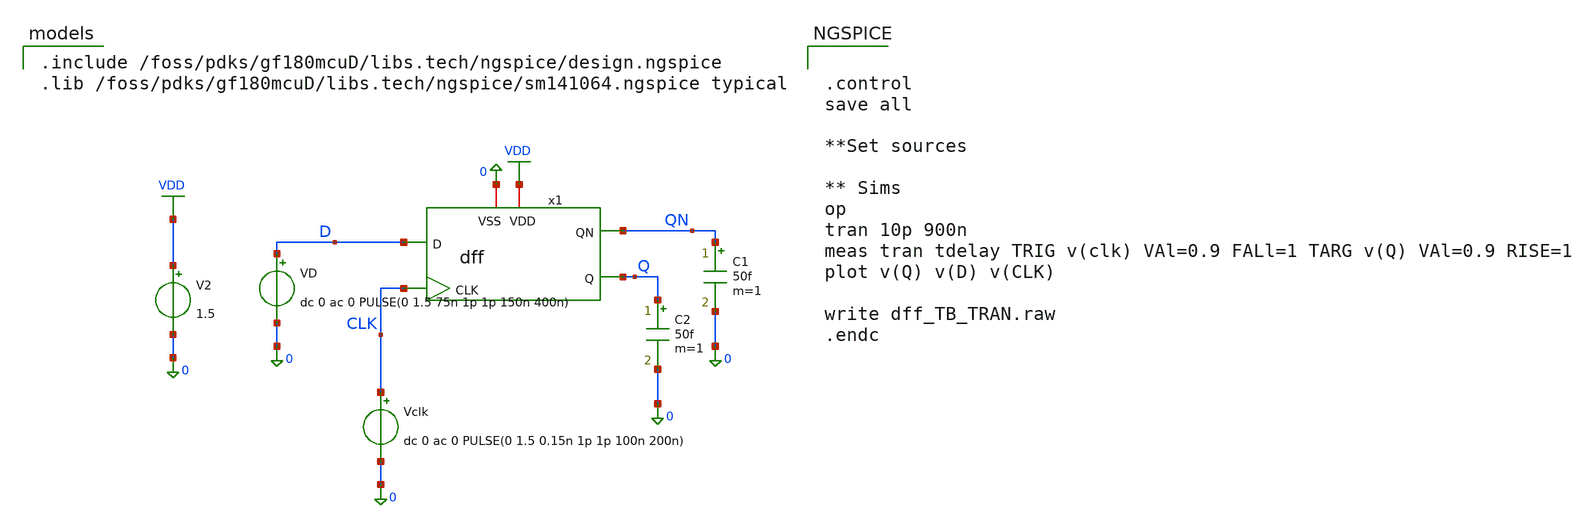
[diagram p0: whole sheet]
** sch_path: designs/DS_modulator/dff/xschem/dff_TB_TRAN.sch
**.subckt dff_TB_TRAN
V2 VDD 0 1.5
Vclk CLK 0 dc 0 ac 0 PULSE(0 1.5 0.15n 1p 1p 100n 200n)
C1 QN 0 50f m=1
C2 Q 0 50f m=1
x1 VDD QN Q CLK 0 D dff
VD D 0 dc 0 ac 0 PULSE(0 1.5 75n 1p 1p 150n 400n)
**** begin user architecture code


.control
save all

**Set sources

** Sims
op
tran 10p 900n
meas tran tdelay TRIG v(clk) VAl=0.9 FALl=1 TARG v(Q) VAl=0.9 RISE=1
plot v(Q) v(D) v(CLK)

write dff_TB_TRAN.raw
.endc



.include /foss/pdks/gf180mcuD/libs.tech/ngspice/design.ngspice
.lib /foss/pdks/gf180mcuD/libs.tech/ngspice/sm141064.ngspice typical

**** end user architecture code
**.ends

* expanding   symbol:  dff.sym # of pins=6
** sym_path: designs/DS_modulator/dff/xschem/dff.sym
** sch_path: designs/DS_modulator/dff/xschem/dff.sch
.subckt dff VDD QN Q CLK VSS D
*.ipin CLK
*.opin QN
*.opin Q
*.ipin D
*.iopin VDD
*.iopin VSS
XM2 CLKN CLK VDD VDD pfet_03v3 L=0.28u W=0.22u nf=1 ad='int((nf+1)/2) * W/nf * 0.18u' as='int((nf+2)/2) * W/nf * 0.18u'
+ pd='2*int((nf+1)/2) * (W/nf + 0.18u)' ps='2*int((nf+2)/2) * (W/nf + 0.18u)' nrd='0.18u / W' nrs='0.18u / W'
+ sa=0 sb=0 sd=0 m=1
XM9 Q CLK net1 VSS nfet_03v3 L=0.28u W=1.5u nf=1 ad='int((nf+1)/2) * W/nf * 0.18u' as='int((nf+2)/2) * W/nf * 0.18u'
+ pd='2*int((nf+1)/2) * (W/nf + 0.18u)' ps='2*int((nf+2)/2) * (W/nf + 0.18u)' nrd='0.18u / W' nrs='0.18u / W'
+ sa=0 sb=0 sd=0 m=1
XM3 QN CLK net2 VSS nfet_03v3 L=0.28u W=1.5u nf=1 ad='int((nf+1)/2) * W/nf * 0.18u' as='int((nf+2)/2) * W/nf * 0.18u'
+ pd='2*int((nf+1)/2) * (W/nf + 0.18u)' ps='2*int((nf+2)/2) * (W/nf + 0.18u)' nrd='0.18u / W' nrs='0.18u / W'
+ sa=0 sb=0 sd=0 m=1
XM4 net2 QM VSS VSS nfet_03v3 L=0.28u W=1.5u nf=1 ad='int((nf+1)/2) * W/nf * 0.18u' as='int((nf+2)/2) * W/nf * 0.18u'
+ pd='2*int((nf+1)/2) * (W/nf + 0.18u)' ps='2*int((nf+2)/2) * (W/nf + 0.18u)' nrd='0.18u / W' nrs='0.18u / W'
+ sa=0 sb=0 sd=0 m=1
XM8 Q QN VSS VSS nfet_03v3 L=0.28u W=0.5u nf=1 ad='int((nf+1)/2) * W/nf * 0.18u' as='int((nf+2)/2) * W/nf * 0.18u'
+ pd='2*int((nf+1)/2) * (W/nf + 0.18u)' ps='2*int((nf+2)/2) * (W/nf + 0.18u)' nrd='0.18u / W' nrs='0.18u / W'
+ sa=0 sb=0 sd=0 m=1
XM10 CLKN CLK VSS VSS nfet_03v3 L=0.28u W=0.22u nf=1 ad='int((nf+1)/2) * W/nf * 0.18u' as='int((nf+2)/2) * W/nf * 0.18u'
+ pd='2*int((nf+1)/2) * (W/nf + 0.18u)' ps='2*int((nf+2)/2) * (W/nf + 0.18u)' nrd='0.18u / W' nrs='0.18u / W'
+ sa=0 sb=0 sd=0 m=1
XM6 net1 QMN VSS VSS nfet_03v3 L=0.28u W=1.5u nf=1 ad='int((nf+1)/2) * W/nf * 0.18u' as='int((nf+2)/2) * W/nf * 0.18u'
+ pd='2*int((nf+1)/2) * (W/nf + 0.18u)' ps='2*int((nf+2)/2) * (W/nf + 0.18u)' nrd='0.18u / W' nrs='0.18u / W'
+ sa=0 sb=0 sd=0 m=1
XM5 QN Q VSS VSS nfet_03v3 L=0.28u W=0.5u nf=1 ad='int((nf+1)/2) * W/nf * 0.18u' as='int((nf+2)/2) * W/nf * 0.18u'
+ pd='2*int((nf+1)/2) * (W/nf + 0.18u)' ps='2*int((nf+2)/2) * (W/nf + 0.18u)' nrd='0.18u / W' nrs='0.18u / W'
+ sa=0 sb=0 sd=0 m=1
XM7 Q QN VDD VDD pfet_03v3 L=0.28u W=1.5u nf=1 ad='int((nf+1)/2) * W/nf * 0.18u' as='int((nf+2)/2) * W/nf * 0.18u'
+ pd='2*int((nf+1)/2) * (W/nf + 0.18u)' ps='2*int((nf+2)/2) * (W/nf + 0.18u)' nrd='0.18u / W' nrs='0.18u / W'
+ sa=0 sb=0 sd=0 m=1
XM1 QN Q VDD VDD pfet_03v3 L=0.28u W=1.5u nf=1 ad='int((nf+1)/2) * W/nf * 0.18u' as='int((nf+2)/2) * W/nf * 0.18u'
+ pd='2*int((nf+1)/2) * (W/nf + 0.18u)' ps='2*int((nf+2)/2) * (W/nf + 0.18u)' nrd='0.18u / W' nrs='0.18u / W'
+ sa=0 sb=0 sd=0 m=1
XM11 DN D VDD VDD pfet_03v3 L=0.28u W=0.22u nf=1 ad='int((nf+1)/2) * W/nf * 0.18u' as='int((nf+2)/2) * W/nf * 0.18u'
+ pd='2*int((nf+1)/2) * (W/nf + 0.18u)' ps='2*int((nf+2)/2) * (W/nf + 0.18u)' nrd='0.18u / W' nrs='0.18u / W'
+ sa=0 sb=0 sd=0 m=1
XM12 QM CLKN net3 VSS nfet_03v3 L=0.28u W=1.5u nf=1 ad='int((nf+1)/2) * W/nf * 0.18u' as='int((nf+2)/2) * W/nf * 0.18u'
+ pd='2*int((nf+1)/2) * (W/nf + 0.18u)' ps='2*int((nf+2)/2) * (W/nf + 0.18u)' nrd='0.18u / W' nrs='0.18u / W'
+ sa=0 sb=0 sd=0 m=1
XM13 QMN CLKN net4 VSS nfet_03v3 L=0.28u W=1.5u nf=1 ad='int((nf+1)/2) * W/nf * 0.18u' as='int((nf+2)/2) * W/nf * 0.18u'
+ pd='2*int((nf+1)/2) * (W/nf + 0.18u)' ps='2*int((nf+2)/2) * (W/nf + 0.18u)' nrd='0.18u / W' nrs='0.18u / W'
+ sa=0 sb=0 sd=0 m=1
XM14 net4 D VSS VSS nfet_03v3 L=0.28u W=1.5u nf=1 ad='int((nf+1)/2) * W/nf * 0.18u' as='int((nf+2)/2) * W/nf * 0.18u'
+ pd='2*int((nf+1)/2) * (W/nf + 0.18u)' ps='2*int((nf+2)/2) * (W/nf + 0.18u)' nrd='0.18u / W' nrs='0.18u / W'
+ sa=0 sb=0 sd=0 m=1
XM15 QM QMN VSS VSS nfet_03v3 L=0.28u W=0.5u nf=1 ad='int((nf+1)/2) * W/nf * 0.18u' as='int((nf+2)/2) * W/nf * 0.18u'
+ pd='2*int((nf+1)/2) * (W/nf + 0.18u)' ps='2*int((nf+2)/2) * (W/nf + 0.18u)' nrd='0.18u / W' nrs='0.18u / W'
+ sa=0 sb=0 sd=0 m=1
XM16 DN D VSS VSS nfet_03v3 L=0.28u W=0.22u nf=1 ad='int((nf+1)/2) * W/nf * 0.18u' as='int((nf+2)/2) * W/nf * 0.18u'
+ pd='2*int((nf+1)/2) * (W/nf + 0.18u)' ps='2*int((nf+2)/2) * (W/nf + 0.18u)' nrd='0.18u / W' nrs='0.18u / W'
+ sa=0 sb=0 sd=0 m=1
XM17 net3 DN VSS VSS nfet_03v3 L=0.28u W=1.5u nf=1 ad='int((nf+1)/2) * W/nf * 0.18u' as='int((nf+2)/2) * W/nf * 0.18u'
+ pd='2*int((nf+1)/2) * (W/nf + 0.18u)' ps='2*int((nf+2)/2) * (W/nf + 0.18u)' nrd='0.18u / W' nrs='0.18u / W'
+ sa=0 sb=0 sd=0 m=1
XM18 QMN QM VSS VSS nfet_03v3 L=0.28u W=0.5u nf=1 ad='int((nf+1)/2) * W/nf * 0.18u' as='int((nf+2)/2) * W/nf * 0.18u'
+ pd='2*int((nf+1)/2) * (W/nf + 0.18u)' ps='2*int((nf+2)/2) * (W/nf + 0.18u)' nrd='0.18u / W' nrs='0.18u / W'
+ sa=0 sb=0 sd=0 m=1
XM19 QM QMN VDD VDD pfet_03v3 L=0.28u W=1.5u nf=1 ad='int((nf+1)/2) * W/nf * 0.18u' as='int((nf+2)/2) * W/nf * 0.18u'
+ pd='2*int((nf+1)/2) * (W/nf + 0.18u)' ps='2*int((nf+2)/2) * (W/nf + 0.18u)' nrd='0.18u / W' nrs='0.18u / W'
+ sa=0 sb=0 sd=0 m=1
XM20 QMN QM VDD VDD pfet_03v3 L=0.28u W=1.5u nf=1 ad='int((nf+1)/2) * W/nf * 0.18u' as='int((nf+2)/2) * W/nf * 0.18u'
+ pd='2*int((nf+1)/2) * (W/nf + 0.18u)' ps='2*int((nf+2)/2) * (W/nf + 0.18u)' nrd='0.18u / W' nrs='0.18u / W'
+ sa=0 sb=0 sd=0 m=1
.ends

.GLOBAL VDD
.end
